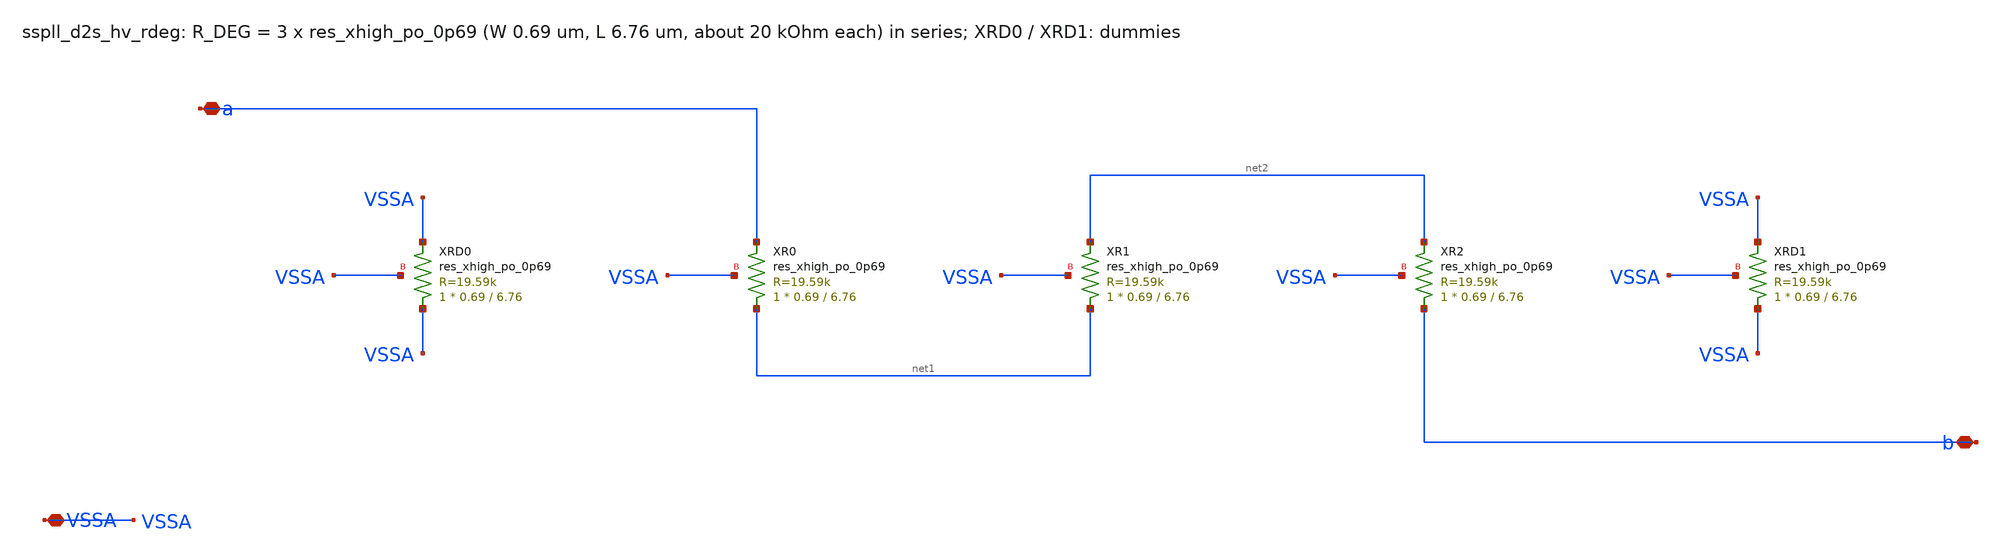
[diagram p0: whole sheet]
** sch_path: xschem/d2s_hv/sspll_d2s_hv_rdeg.sch
**.subckt sspll_d2s_hv_rdeg a b VSSA
*.iopin a
*.iopin b
*.iopin VSSA
XXRD0 VSSA VSSA VSSA sky130_fd_pr__res_xhigh_po_0p69 L=6.76 mult=1 m=1
XXR0 net1 a VSSA sky130_fd_pr__res_xhigh_po_0p69 L=6.76 mult=1 m=1
XXR1 net1 net2 VSSA sky130_fd_pr__res_xhigh_po_0p69 L=6.76 mult=1 m=1
XXR2 b net2 VSSA sky130_fd_pr__res_xhigh_po_0p69 L=6.76 mult=1 m=1
XXRD1 VSSA VSSA VSSA sky130_fd_pr__res_xhigh_po_0p69 L=6.76 mult=1 m=1
**.ends
.end
